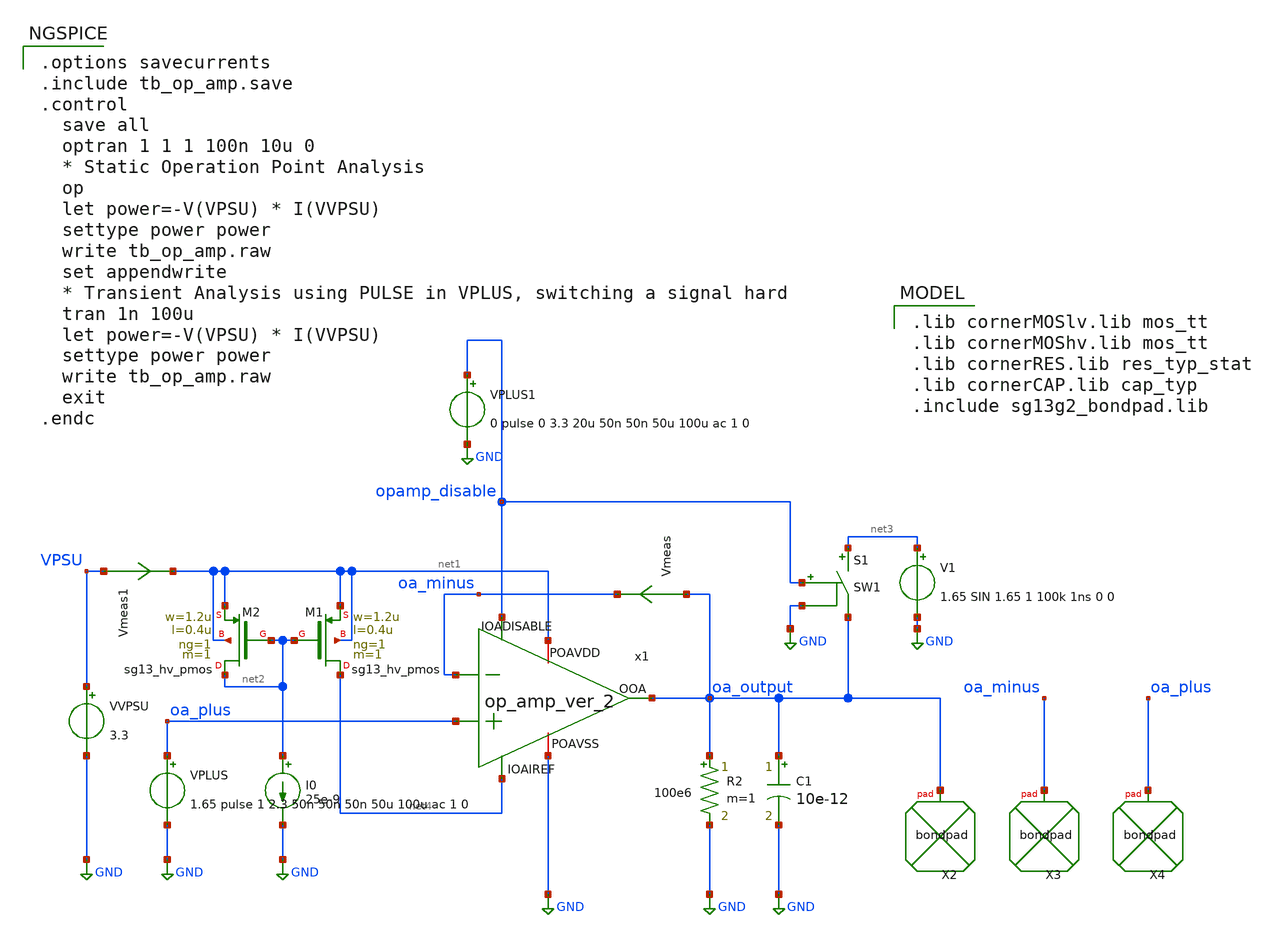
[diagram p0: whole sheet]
** sch_path: xschem/op_amp_tb.sch
**.subckt op_amp_tb
VVPSU VPSU GND 3.3
I0 net2 GND 25e-9
VPLUS oa_plus GND 1.65 pulse 1 2.3 50n 50n 50n 50u 100u ac 1 0
R2 oa_output GND 100e6 m=1
C1 oa_output GND 10e-12 m=1
Vmeas oa_output oa_minus 0
.save i(vmeas)
XX2 oa_output bondpad size=80u shape=0 padtype=0
XX3 oa_minus bondpad size=80u shape=0 padtype=0
XX4 oa_plus bondpad size=80u shape=0 padtype=0
VPLUS1 opamp_disable GND 0 pulse 0 3.3 20u 50n 50n 50u 100u ac 1 0
XM1 net4 net2 net1 net1 sg13_hv_pmos w=1.2u l=0.4u ng=1 m=1 mm_ok=1
XM2 net2 net2 net1 net1 sg13_hv_pmos w=1.2u l=0.4u ng=1 m=1 mm_ok=1
V1 net3 GND 1.65 SIN 1.65 1 100k 1ns 0 0
S1 net3 oa_output opamp_disable GND SW1
Vmeas1 VPSU net1 0
.save i(vmeas1)
x1 net1 net4 oa_minus oa_output oa_plus GND opamp_disable op_amp_ver_2
**** begin user architecture code

.lib cornerMOSlv.lib mos_tt
.lib cornerMOShv.lib mos_tt
.lib cornerRES.lib res_typ_stat
.lib cornerCAP.lib cap_typ
.include sg13g2_bondpad.lib



.options savecurrents
.include tb_op_amp.save
.control
  save all
  optran 1 1 1 100n 10u 0
  * Static Operation Point Analysis
  op
  let power=-V(VPSU) * I(VVPSU)
  settype power power
  write tb_op_amp.raw
  set appendwrite
  * Transient Analysis using PULSE in VPLUS, switching a signal hard
  tran 1n 100u
  let power=-V(VPSU) * I(VVPSU)
  settype power power
  write tb_op_amp.raw
  exit
.endc


**** end user architecture code
**.ends

* expanding   symbol:  op_amp_ver_2.sym # of pins=7
** sym_path: xschem/op_amp_ver_2.sym
** sch_path: xschem/op_amp_ver_2.sch
.subckt op_amp_ver_2 POAVDD IOAIREF IOAM OOA IOAP POAVSS IOADISABLE
*.iopin POAVDD
*.ipin IOAM
*.ipin IOAP
*.opin OOA
*.ipin IOAIREF
*.iopin POAVSS
*.ipin IOADISABLE
XMP13 net1 net1 POAVDD POAVDD sg13_hv_pmos w=2.4u l=0.4u ng=1 m=1 mm_ok=1
XMP14 ptlg ptlg net1 POAVDD sg13_hv_pmos w=2.4u l=0.4u ng=1 m=1 mm_ok=1
XMN16 ptlg ncasc net2 POAVSS sg13_hv_nmos w=0.6u l=0.6u ng=1 m=1 mm_ok=1
XMN13 net2 nbias POAVSS POAVSS sg13_hv_nmos w=0.6u l=2.4u ng=1 m=1 mm_ok=1
XMN18 ntlg ntlg net3 POAVSS sg13_hv_nmos w=1.2u l=0.6u ng=1 m=1 mm_ok=1
XMN17 net3 net3 POAVSS POAVSS sg13_hv_nmos w=1.2u l=0.6u ng=1 m=1 mm_ok=1
XMP10 net11 pbias POAVDD POAVDD sg13_hv_pmos w=1.2u l=1.2u ng=1 m=1 mm_ok=1
XMP12 ntlg pcasc net11 POAVDD sg13_hv_pmos w=1.2u l=0.6u ng=1 m=1 mm_ok=1
XMP1 net9 pbias POAVDD POAVDD sg13_hv_pmos w=1.2u l=1.2u ng=1 m=4 mm_ok=1
XMP2 net10 pbias POAVDD POAVDD sg13_hv_pmos w=1.2u l=1.2u ng=1 m=4 mm_ok=1
XMN1 net9 IOAM net5 POAVSS sg13_hv_nmos w=4.8u l=0.45u ng=1 m=1 mm_ok=1
XMN2 net10 IOAP net5 POAVSS sg13_hv_nmos w=4.8u l=0.45u ng=1 m=1 mm_ok=1
XMN3 net4 nbias POAVSS POAVSS sg13_hv_nmos w=0.6u l=2.4u ng=1 m=8 mm_ok=1
XMN6 net5 ncasc net4 POAVSS sg13_hv_nmos w=0.6u l=0.6u ng=1 m=8 mm_ok=1
XMN7 net8 ncasc net7 POAVSS sg13_hv_nmos w=0.6u l=0.6u ng=1 m=8 mm_ok=1
XMN8 ndrive ncasc net6 POAVSS sg13_hv_nmos w=0.6u l=0.6u ng=1 m=8 mm_ok=1
XMN4 net7 net8 POAVSS POAVSS sg13_hv_nmos w=0.6u l=2.4u ng=1 m=8 mm_ok=1
XMN5 net6 net8 POAVSS POAVSS sg13_hv_nmos w=0.6u l=2.4u ng=1 m=8 mm_ok=1
XMP3 net9 pbias POAVDD POAVDD sg13_hv_pmos w=1.2u l=1.2u ng=1 m=4 mm_ok=1
XMP5 net8 pcasc net9 POAVDD sg13_hv_pmos w=1.2u l=0.6u ng=1 m=8 mm_ok=1
XMP4 net10 pbias POAVDD POAVDD sg13_hv_pmos w=1.2u l=1.2u ng=1 m=4 mm_ok=1
XMP6 pdrive pcasc net10 POAVDD sg13_hv_pmos w=1.2u l=0.6u ng=1 m=8 mm_ok=1
XMP7 ndrive ptlg pdrive POAVDD sg13_hv_pmos w=2.4u l=0.4u ng=1 m=4 mm_ok=1
XMN9 pdrive ntlg ndrive POAVSS sg13_hv_nmos w=1.2u l=0.6u ng=1 m=4 mm_ok=1
XMP8 OOA pdrive POAVDD POAVDD sg13_hv_pmos w=2.4u l=0.4u ng=1 m=40 mm_ok=1
XMN10 OOA ndrive POAVSS POAVSS sg13_hv_nmos w=1.2u l=0.6u ng=1 m=40 mm_ok=1
XC2 OOA ndrive cap_cmim w=28.570e-6 l=14e-6 m=1 mm_ok=1
XC1 OOA pdrive cap_cmim w=28.570e-6 l=14e-6 m=1 mm_ok=1
XMN20 IOAIREF IOAIREF POAVSS POAVSS sg13_hv_nmos w=0.6u l=2.4u ng=1 m=1 mm_ok=1
XMN21 pcasc IOAIREF POAVSS POAVSS sg13_hv_nmos w=0.6u l=2.4u ng=1 m=1 mm_ok=1
XMN22 pbias IOAIREF POAVSS POAVSS sg13_hv_nmos w=0.6u l=2.4u ng=1 m=1 mm_ok=1
XMN23 net19 ncasc POAVSS POAVSS sg13_hv_nmos w=0.4u l=10u ng=1 m=1 mm_ok=1
XMN25 net13 nbias POAVSS POAVSS sg13_hv_nmos w=0.6u l=2.4u ng=1 m=1 mm_ok=1
XMN24 ncasc ncasc net22 POAVSS sg13_hv_nmos w=0.4u l=10u ng=1 m=1 mm_ok=1
XMN26 nbias ncasc net13 POAVSS sg13_hv_nmos w=0.6u l=0.6u ng=1 m=1 mm_ok=1
XMP21 pcasc pcasc net18 POAVDD sg13_hv_pmos w=1u l=10u ng=1 m=1 mm_ok=1
XMP20 net18 pcasc net17 POAVDD sg13_hv_pmos w=1u l=10.0u ng=1 m=1 mm_ok=1
XMP22 net12 pbias POAVDD POAVDD sg13_hv_pmos w=1.2u l=1.2u ng=1 m=1 mm_ok=1
XMP25 pbias pcasc net12 POAVDD sg13_hv_pmos w=1.2u l=0.6u ng=1 m=1 mm_ok=1
XMP26 ncasc pcasc net15 POAVDD sg13_hv_pmos w=1.2u l=0.6u ng=1 m=1 mm_ok=1
XMP23 net15 pbias POAVDD POAVDD sg13_hv_pmos w=1.2u l=1.2u ng=1 m=1 mm_ok=1
XMP24 net14 pbias POAVDD POAVDD sg13_hv_pmos w=1.2u l=1.2u ng=1 m=1 mm_ok=1
XMP27 nbias pcasc net14 POAVDD sg13_hv_pmos w=1.2u l=0.6u ng=1 m=1 mm_ok=1
XMP16 net17 pcasc net16 POAVDD sg13_hv_pmos w=1u l=10.0u ng=1 m=1 mm_ok=1
XMN11 net20 ncasc net19 POAVSS sg13_hv_nmos w=0.4u l=10u ng=1 m=1 mm_ok=1
XMP28 net16 pcasc POAVDD POAVDD sg13_hv_pmos w=1u l=10.0u ng=1 m=1 mm_ok=1
XMN12 net21 ncasc net20 POAVSS sg13_hv_nmos w=0.4u l=10u ng=1 m=1 mm_ok=1
XMN14 net22 ncasc net21 POAVSS sg13_hv_nmos w=0.4u l=10u ng=1 m=1 mm_ok=1
XMDP1 POAVDD pbias POAVDD POAVDD sg13_hv_pmos w=1.2u l=1.2u ng=1 m=1 mm_ok=1
XMDP2 POAVDD pbias POAVDD POAVDD sg13_hv_pmos w=1.2u l=1.2u ng=1 m=1 mm_ok=1
XMDOP1 POAVDD pcasc POAVDD POAVDD sg13_hv_pmos w=1.2u l=0.6u ng=1 m=1 mm_ok=1
XMDOP2 POAVDD pcasc POAVDD POAVDD sg13_hv_pmos w=1.2u l=0.6u ng=1 m=1 mm_ok=1
XMDOP3 POAVDD pcasc POAVDD POAVDD sg13_hv_pmos w=1.2u l=0.6u ng=1 m=1 mm_ok=1
XMDOP4 POAVDD pcasc POAVDD POAVDD sg13_hv_pmos w=1.2u l=0.6u ng=1 m=1 mm_ok=1
XMDN1 POAVSS nbias POAVSS POAVSS sg13_hv_nmos w=0.6u l=2.4u ng=1 m=1 mm_ok=1
XMDN2 POAVSS nbias POAVSS POAVSS sg13_hv_nmos w=0.6u l=2.4u ng=1 m=1 mm_ok=1
XMDON1 nIOADISABLE IOADISABLE POAVSS POAVSS sg13_hv_nmos w=0.6u l=0.6u ng=1 m=1 mm_ok=1
XMDON2 ntlg IOADISABLE POAVSS POAVSS sg13_hv_nmos w=0.6u l=0.6u ng=1 m=1 mm_ok=1
XMDON3 ndrive IOADISABLE POAVSS POAVSS sg13_hv_nmos w=0.6u l=0.6u ng=1 m=1 mm_ok=1
XMDON4 IOAIREF IOADISABLE POAVSS POAVSS sg13_hv_nmos w=0.6u l=0.6u ng=1 m=1 mm_ok=1
XMDP7 POAVDD pbias POAVDD POAVDD sg13_hv_pmos w=1.2u l=1.2u ng=1 m=1 mm_ok=1
XMDP8 POAVDD pbias POAVDD POAVDD sg13_hv_pmos w=1.2u l=1.2u ng=1 m=1 mm_ok=1
XMDN7 POAVSS nbias POAVSS POAVSS sg13_hv_nmos w=0.6u l=2.4u ng=1 m=1 mm_ok=1
XMDN8 POAVSS nbias POAVSS POAVSS sg13_hv_nmos w=0.6u l=2.4u ng=1 m=1 mm_ok=1
XMDN9 POAVSS POAVSS POAVSS POAVSS sg13_hv_nmos w=1.2u l=0.45u ng=1 m=1 mm_ok=1
XMDN10 POAVSS POAVSS POAVSS POAVSS sg13_hv_nmos w=1.2u l=0.45u ng=1 m=1 mm_ok=1
XMDN11 POAVSS POAVSS POAVSS POAVSS sg13_hv_nmos w=1.2u l=0.45u ng=1 m=1 mm_ok=1
XMDN12 POAVSS POAVSS POAVSS POAVSS sg13_hv_nmos w=1.2u l=0.45u ng=1 m=1 mm_ok=1
XMDN13 POAVSS POAVSS POAVSS POAVSS sg13_hv_nmos w=2.4u l=0.45u ng=1 m=1 mm_ok=1
XMDN14 POAVSS POAVSS POAVSS POAVSS sg13_hv_nmos w=2.4u l=0.45u ng=1 m=1 mm_ok=1
XMDN15 POAVSS POAVSS POAVSS POAVSS sg13_hv_nmos w=2.4u l=0.45u ng=1 m=1 mm_ok=1
XMDN16 POAVSS POAVSS POAVSS POAVSS sg13_hv_nmos w=2.4u l=0.45u ng=1 m=1 mm_ok=1
XMDN17 POAVSS POAVSS POAVSS POAVSS sg13_hv_nmos w=1.2u l=0.45u ng=1 m=1 mm_ok=1
XMDN18 POAVSS POAVSS POAVSS POAVSS sg13_hv_nmos w=1.2u l=0.45u ng=1 m=1 mm_ok=1
XMDN19 POAVSS POAVSS POAVSS POAVSS sg13_hv_nmos w=1.2u l=0.45u ng=1 m=1 mm_ok=1
XMDN20 POAVSS POAVSS POAVSS POAVSS sg13_hv_nmos w=1.2u l=0.45u ng=1 m=1 mm_ok=1
XMDN21 POAVSS IOAIREF POAVSS POAVSS sg13_hv_nmos w=0.6u l=2.4u ng=1 m=1 mm_ok=1
XMDN22 POAVSS IOAIREF POAVSS POAVSS sg13_hv_nmos w=0.6u l=2.4u ng=1 m=1 mm_ok=1
XMDP9 POAVDD pcasc POAVDD POAVDD sg13_hv_pmos w=1u l=10u ng=1 m=1 mm_ok=1
XMDN23 POAVSS ncasc POAVSS POAVSS sg13_hv_nmos w=0.4u l=10u ng=1 m=1 mm_ok=1
XMDP10 POAVDD pcasc POAVDD POAVDD sg13_hv_pmos w=1u l=10u ng=1 m=1 mm_ok=1
XMDN24 POAVSS ncasc POAVSS POAVSS sg13_hv_nmos w=0.4u l=10u ng=1 m=1 mm_ok=1
XMDP11 POAVDD pbias POAVDD POAVDD sg13_hv_pmos w=1.2u l=1.2u ng=1 m=1 mm_ok=1
XMDP12 POAVDD pbias POAVDD POAVDD sg13_hv_pmos w=1.2u l=1.2u ng=1 m=1 mm_ok=1
XMDP13 POAVDD pcasc POAVDD POAVDD sg13_hv_pmos w=1.2u l=0.6u ng=1 m=1 mm_ok=1
XMDP14 POAVDD pcasc POAVDD POAVDD sg13_hv_pmos w=1.2u l=0.6u ng=1 m=1 mm_ok=1
XMDN25 POAVSS POAVSS POAVSS POAVSS sg13_hv_nmos w=0.6u l=2.4u ng=1 m=1 mm_ok=1
XMDN26 POAVSS POAVSS POAVSS POAVSS sg13_hv_nmos w=0.6u l=2.4u ng=1 m=1 mm_ok=1
XMDN27 POAVSS ncasc POAVSS POAVSS sg13_hv_nmos w=0.6u l=0.6u ng=1 m=1 mm_ok=1
XMDN28 POAVSS ncasc POAVSS POAVSS sg13_hv_nmos w=0.6u l=0.6u ng=1 m=1 mm_ok=1
XMDP15 POAVDD POAVDD POAVDD POAVDD sg13_hv_pmos w=2.4u l=0.4u ng=1 m=8 mm_ok=1
XMDN29 POAVSS POAVSS POAVSS POAVSS sg13_hv_nmos w=1.2u l=0.6u ng=1 m=8 mm_ok=1
XMDP16 POAVDD POAVDD POAVDD POAVDD sg13_hv_pmos w=2.4u l=0.4u ng=1 m=2 mm_ok=1
XMDN30 POAVSS POAVSS POAVSS POAVSS sg13_hv_nmos w=1.2u l=0.6u ng=1 m=2 mm_ok=1
XMDP17 POAVDD POAVDD POAVDD POAVDD sg13_hv_pmos w=2.4u l=0.4u ng=1 m=8 mm_ok=1
XMDN31 POAVSS POAVSS POAVSS POAVSS sg13_hv_nmos w=1.2u l=0.6u ng=1 m=8 mm_ok=1
XMDOP5 nIOADISABLE IOADISABLE POAVDD POAVDD sg13_hv_pmos w=1.2u l=0.6u ng=1 m=1 mm_ok=1
XMDOP6 ptlg nIOADISABLE POAVDD POAVDD sg13_hv_pmos w=1.2u l=0.6u ng=1 m=1 mm_ok=1
XMDOP7 pdrive nIOADISABLE POAVDD POAVDD sg13_hv_pmos w=1.2u l=0.6u ng=1 m=1 mm_ok=1
XMDOP8 pcasc nIOADISABLE POAVDD POAVDD sg13_hv_pmos w=1.2u l=0.6u ng=1 m=1 mm_ok=1
.ends

.GLOBAL GND
**** begin user architecture code
.MODEL SW1 SW   VT=3 VH=0.01  RON=1k ROFF=10G
**** end user architecture code
.end
